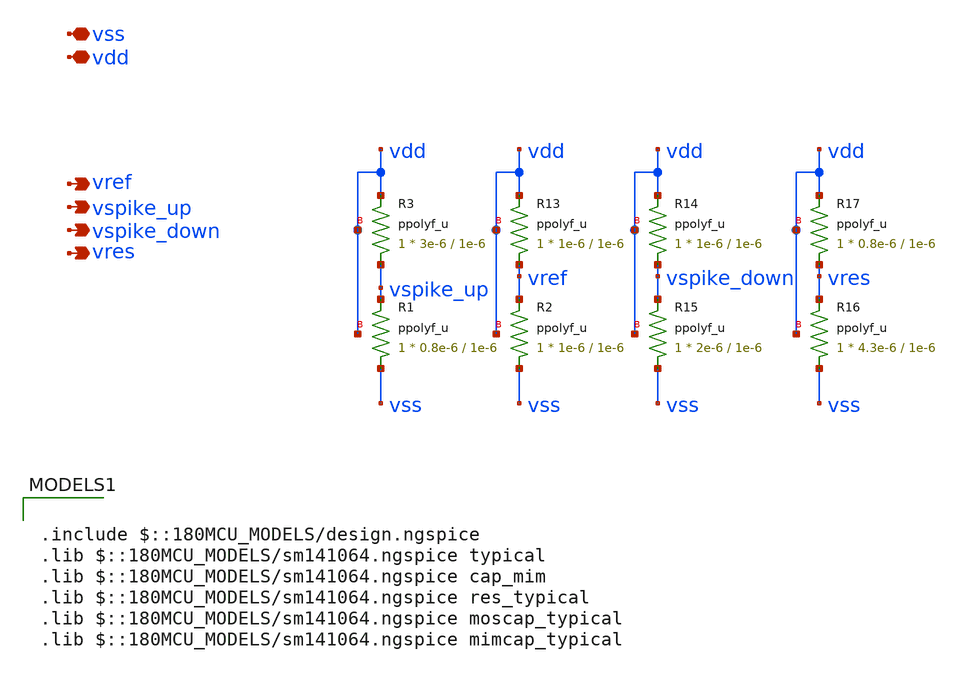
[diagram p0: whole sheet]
** sch_path: designs/libs/core_LIF_comp/core_vdiv/vdiv.sch
**.subckt vdiv vref vdd vss vspike_up vspike_down vres
*.opin vref
*.iopin vdd
*.iopin vss
*.opin vspike_up
*.opin vspike_down
*.opin vres
XR3 vspike_up vdd vdd ppolyf_u r_width=3e-6 r_length=1e-6 m=1
XR1 vss vspike_up vdd ppolyf_u r_width=0.8e-6 r_length=1e-6 m=1
XR2 vss vref vdd ppolyf_u r_width=1e-6 r_length=1e-6 m=1
XR13 vref vdd vdd ppolyf_u r_width=1e-6 r_length=1e-6 m=1
XR14 vspike_down vdd vdd ppolyf_u r_width=1e-6 r_length=1e-6 m=1
XR15 vss vspike_down vdd ppolyf_u r_width=2e-6 r_length=1e-6 m=1
XR16 vss vres vdd ppolyf_u r_width=4.3e-6 r_length=1e-6 m=1
XR17 vres vdd vdd ppolyf_u r_width=0.8e-6 r_length=1e-6 m=1
**** begin user architecture code

.include $::180MCU_MODELS/design.ngspice
.lib $::180MCU_MODELS/sm141064.ngspice typical
.lib $::180MCU_MODELS/sm141064.ngspice cap_mim
.lib $::180MCU_MODELS/sm141064.ngspice res_typical
.lib $::180MCU_MODELS/sm141064.ngspice moscap_typical
.lib $::180MCU_MODELS/sm141064.ngspice mimcap_typical

**** end user architecture code
**.ends
.end
